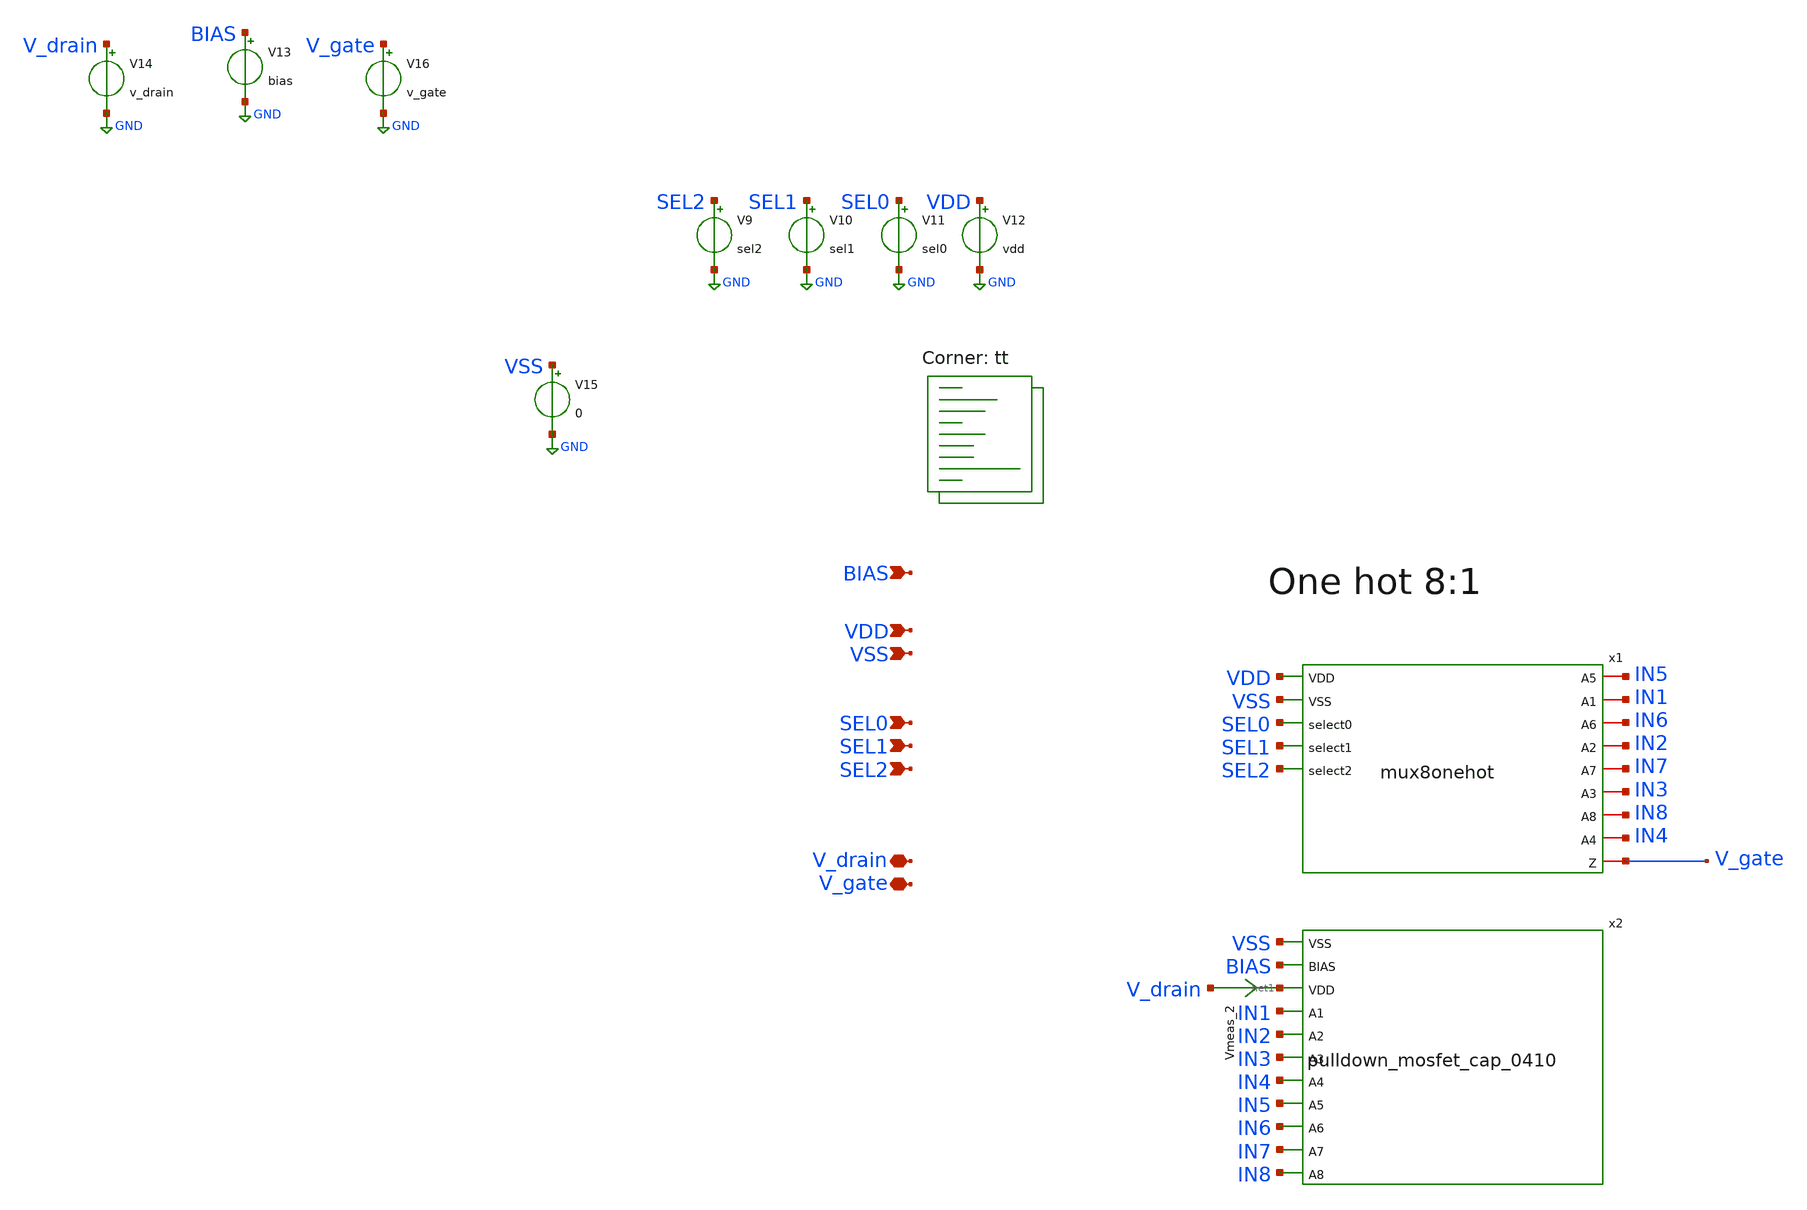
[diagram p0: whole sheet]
** sch_path: sch/tb_mux8onehot_cap_0410.sch
**.subckt tb_mux8onehot_cap_0410 SEL0 SEL1 SEL2 VDD VSS V_gate BIAS V_drain
*.ipin SEL0
*.ipin SEL1
*.ipin SEL2
*.ipin VDD
*.ipin VSS
*.iopin V_gate
*.ipin BIAS
*.iopin V_drain
x1 VDD VSS SEL0 SEL1 IN5 SEL2 IN1 IN6 IN2 IN7 IN3 IN8 IN4 V_gate mux8onehot
x2 VSS BIAS net1 IN1 IN2 IN3 IN4 IN5 IN6 IN7 IN8 pulldown_mosfet_cap_0410
V9 SEL2 GND sel2
V10 SEL1 GND sel1
V11 SEL0 GND sel0
V12 VDD GND vdd
V15 VSS GND 0
V13 BIAS GND bias
V14 V_drain GND v_drain
V16 V_gate GND v_gate
Vmeas_2 V_drain net1 0
.save i(vmeas_2)
**** begin user architecture code



.include /home/isshu/pdk/ciel/sky130/versions/0fe599b2afb6708d281543108caf8310912f54af/sky130A/libs.ref/sky130_fd_sc_hd/spice/sky130_fd_sc_hd.spice
.param vdd = 1.8
.param SRCRES = 1k
.param sel0 = 1.8
.param sel1 = 1.8
.param sel2 = 1.8

.param bias = 0.8
.param v_drain = 1.8
.param v_gate = 0


.options savecurrents


.control
set filetype=ascii
save all

* V_drainの初期値、ステップ、終了値を設定
let vd_val = 0
let vd_step = 0.2
let vd_stop = 0.4

* ループ処理でトランジェント解析を繰り返す
while vd_val <= vd_stop
    alter V16 vd_val
    tran 100p 50n
    let vd_val = vd_val + vd_step
end

* 複数回のrun結果がまとめて出力されます
print all >> simulation_log_mux8onehot_cap_0410_Vdrain.txt
wrdata tb_mux8onehot_cap_0410_Vdrain.dat all
write tb_mux8onehot_cap_0410_Vdrain.raw all
.endc



.lib $::SKYWATER_MODELS/sky130.lib.spice tt
**** end user architecture code
**.ends
.GLOBAL GND
.end
